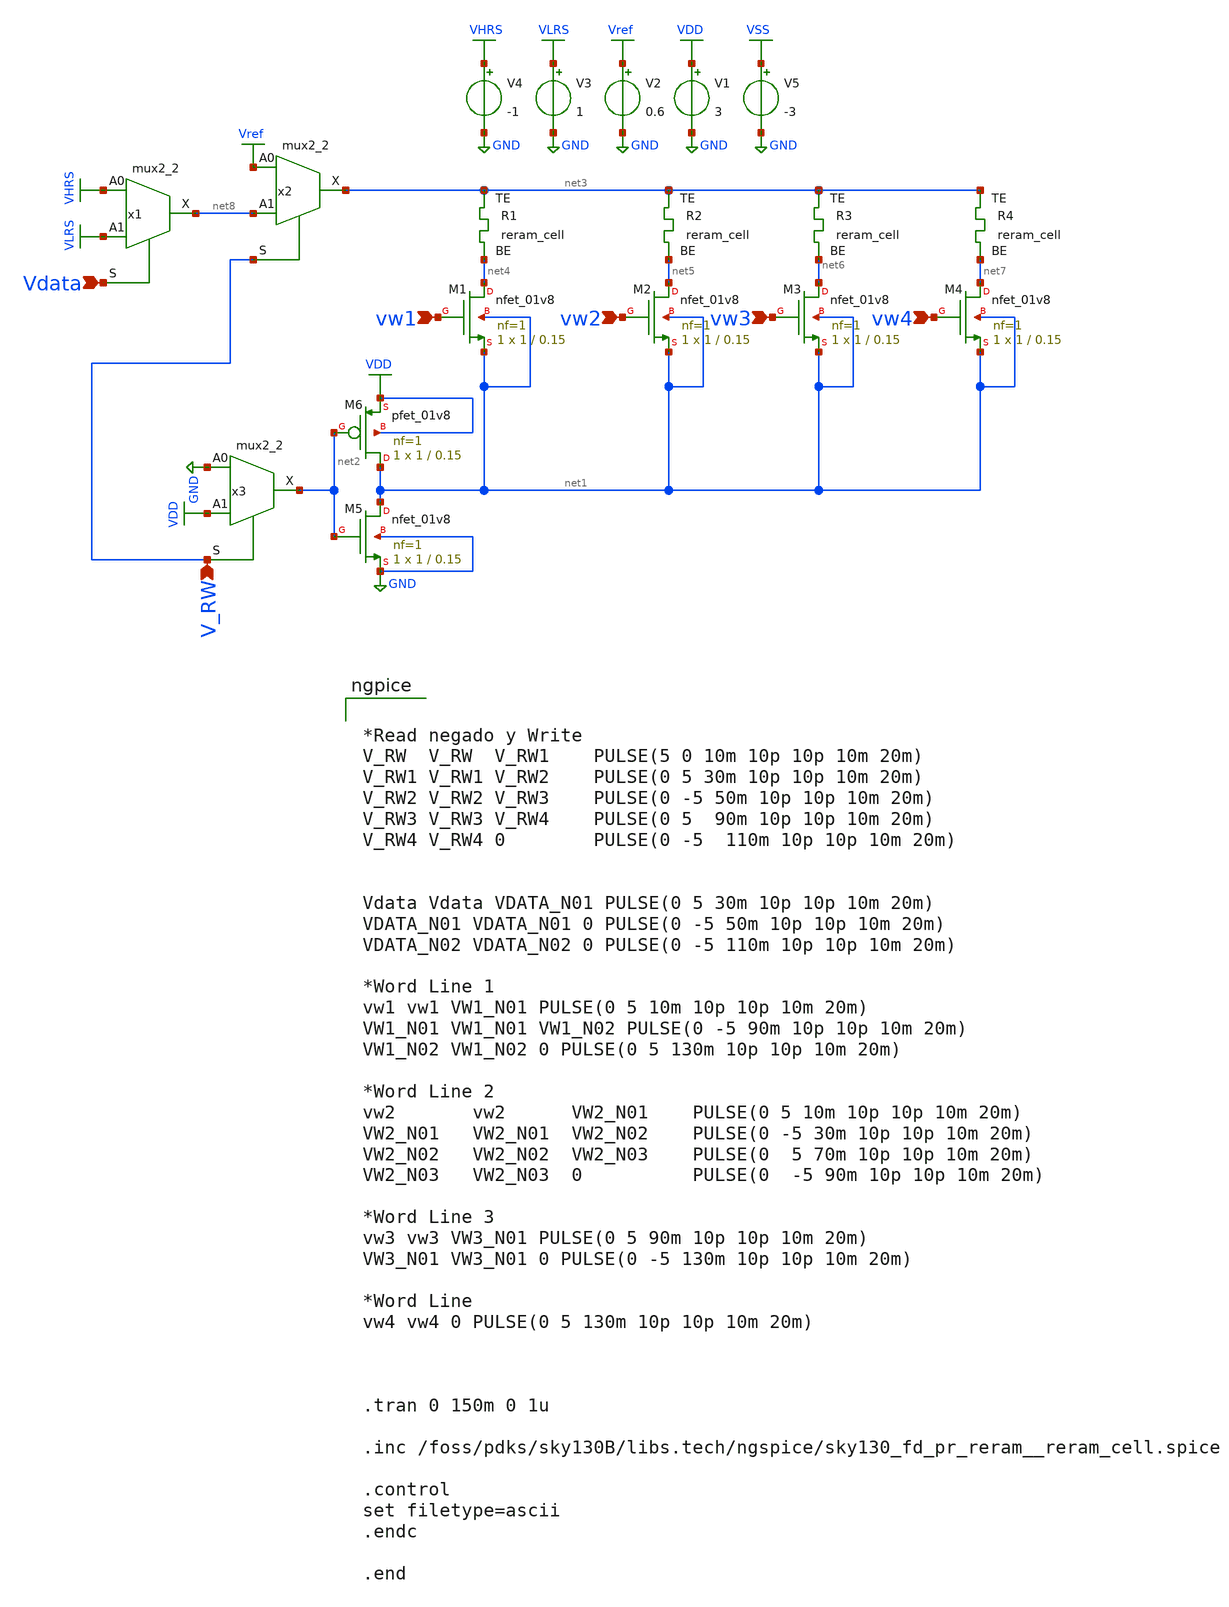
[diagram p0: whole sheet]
** sch_path: xschem/CrossBar.sch
**.subckt CrossBar vw1 vw2 vw3 vw4 Vdata V_RW
*.ipin vw1
*.ipin vw2
*.ipin vw3
*.ipin vw4
*.ipin Vdata
*.ipin V_RW
x1 VHRS VLRS Vdata GND VSS VDD VGND net8 sky130_fd_sc_hd__mux2_2
x2 Vref net8 V_RW GND VSS VDD GND net3 sky130_fd_sc_hd__mux2_2
x3 GND VDD V_RW GND GND VSS GND net2 sky130_fd_sc_hd__mux2_2
XR1 net3 net4 sky130_fd_pr_reram__reram_cell Tfilament_0=3.3e-9
XR2 net3 net5 sky130_fd_pr_reram__reram_cell Tfilament_0=3.3e-9
XR3 net3 net6 sky130_fd_pr_reram__reram_cell Tfilament_0=3.3e-9
XR4 net3 net7 sky130_fd_pr_reram__reram_cell Tfilament_0=3.3e-9
XM1 net4 vw1 net1 net1 sky130_fd_pr__nfet_01v8 L=0.15 W=1 nf=1 ad='int((nf+1)/2) * W/nf * 0.29' as='int((nf+2)/2) * W/nf * 0.29'
+ pd='2*int((nf+1)/2) * (W/nf + 0.29)' ps='2*int((nf+2)/2) * (W/nf + 0.29)' nrd='0.29 / W' nrs='0.29 / W'
+ sa=0 sb=0 sd=0 mult=1 m=1
XM2 net5 vw2 net1 net1 sky130_fd_pr__nfet_01v8 L=0.15 W=1 nf=1 ad='int((nf+1)/2) * W/nf * 0.29' as='int((nf+2)/2) * W/nf * 0.29'
+ pd='2*int((nf+1)/2) * (W/nf + 0.29)' ps='2*int((nf+2)/2) * (W/nf + 0.29)' nrd='0.29 / W' nrs='0.29 / W'
+ sa=0 sb=0 sd=0 mult=1 m=1
XM3 net6 vw3 net1 net1 sky130_fd_pr__nfet_01v8 L=0.15 W=1 nf=1 ad='int((nf+1)/2) * W/nf * 0.29' as='int((nf+2)/2) * W/nf * 0.29'
+ pd='2*int((nf+1)/2) * (W/nf + 0.29)' ps='2*int((nf+2)/2) * (W/nf + 0.29)' nrd='0.29 / W' nrs='0.29 / W'
+ sa=0 sb=0 sd=0 mult=1 m=1
XM4 net7 vw4 net1 net1 sky130_fd_pr__nfet_01v8 L=0.15 W=1 nf=1 ad='int((nf+1)/2) * W/nf * 0.29' as='int((nf+2)/2) * W/nf * 0.29'
+ pd='2*int((nf+1)/2) * (W/nf + 0.29)' ps='2*int((nf+2)/2) * (W/nf + 0.29)' nrd='0.29 / W' nrs='0.29 / W'
+ sa=0 sb=0 sd=0 mult=1 m=1
XM5 net1 net2 GND GND sky130_fd_pr__nfet_01v8 L=0.15 W=1 nf=1 ad='int((nf+1)/2) * W/nf * 0.29' as='int((nf+2)/2) * W/nf * 0.29'
+ pd='2*int((nf+1)/2) * (W/nf + 0.29)' ps='2*int((nf+2)/2) * (W/nf + 0.29)' nrd='0.29 / W' nrs='0.29 / W'
+ sa=0 sb=0 sd=0 mult=1 m=1
XM6 net1 net2 VDD VDD sky130_fd_pr__pfet_01v8 L=0.15 W=1 nf=1 ad='int((nf+1)/2) * W/nf * 0.29' as='int((nf+2)/2) * W/nf * 0.29'
+ pd='2*int((nf+1)/2) * (W/nf + 0.29)' ps='2*int((nf+2)/2) * (W/nf + 0.29)' nrd='0.29 / W' nrs='0.29 / W'
+ sa=0 sb=0 sd=0 mult=1 m=1
V1 VDD GND 3
V2 Vref GND 0.6
V3 VLRS GND 1
V4 VHRS GND -1
V5 VSS GND -3
**** begin user architecture code


*Read negado y Write
V_RW  V_RW  V_RW1    PULSE(5 0 10m 10p 10p 10m 20m)
V_RW1 V_RW1 V_RW2    PULSE(0 5 30m 10p 10p 10m 20m)
V_RW2 V_RW2 V_RW3    PULSE(0 -5 50m 10p 10p 10m 20m)
V_RW3 V_RW3 V_RW4    PULSE(0 5  90m 10p 10p 10m 20m)
V_RW4 V_RW4 0        PULSE(0 -5  110m 10p 10p 10m 20m)


Vdata Vdata VDATA_N01 PULSE(0 5 30m 10p 10p 10m 20m)
VDATA_N01 VDATA_N01 0 PULSE(0 -5 50m 10p 10p 10m 20m)
VDATA_N02 VDATA_N02 0 PULSE(0 -5 110m 10p 10p 10m 20m)

*Word Line 1
vw1 vw1 VW1_N01 PULSE(0 5 10m 10p 10p 10m 20m)
VW1_N01 VW1_N01 VW1_N02 PULSE(0 -5 90m 10p 10p 10m 20m)
VW1_N02 VW1_N02 0 PULSE(0 5 130m 10p 10p 10m 20m)

*Word Line 2
vw2       vw2      VW2_N01    PULSE(0 5 10m 10p 10p 10m 20m)
VW2_N01   VW2_N01  VW2_N02    PULSE(0 -5 30m 10p 10p 10m 20m)
VW2_N02   VW2_N02  VW2_N03    PULSE(0  5 70m 10p 10p 10m 20m)
VW2_N03   VW2_N03  0          PULSE(0  -5 90m 10p 10p 10m 20m)

*Word Line 3
vw3 vw3 VW3_N01 PULSE(0 5 90m 10p 10p 10m 20m)
VW3_N01 VW3_N01 0 PULSE(0 -5 130m 10p 10p 10m 20m)

*Word Line
vw4 vw4 0 PULSE(0 5 130m 10p 10p 10m 20m)



.tran 0 150m 0 1u

.inc /foss/pdks/sky130B/libs.tech/ngspice/sky130_fd_pr_reram__reram_cell.spice

.control
set filetype=ascii
.endc

.end

**** end user architecture code
**.ends
.GLOBAL VDD
.GLOBAL GND
.GLOBAL Vref
.GLOBAL VHRS
.GLOBAL VLRS
.GLOBAL VSS
.end
